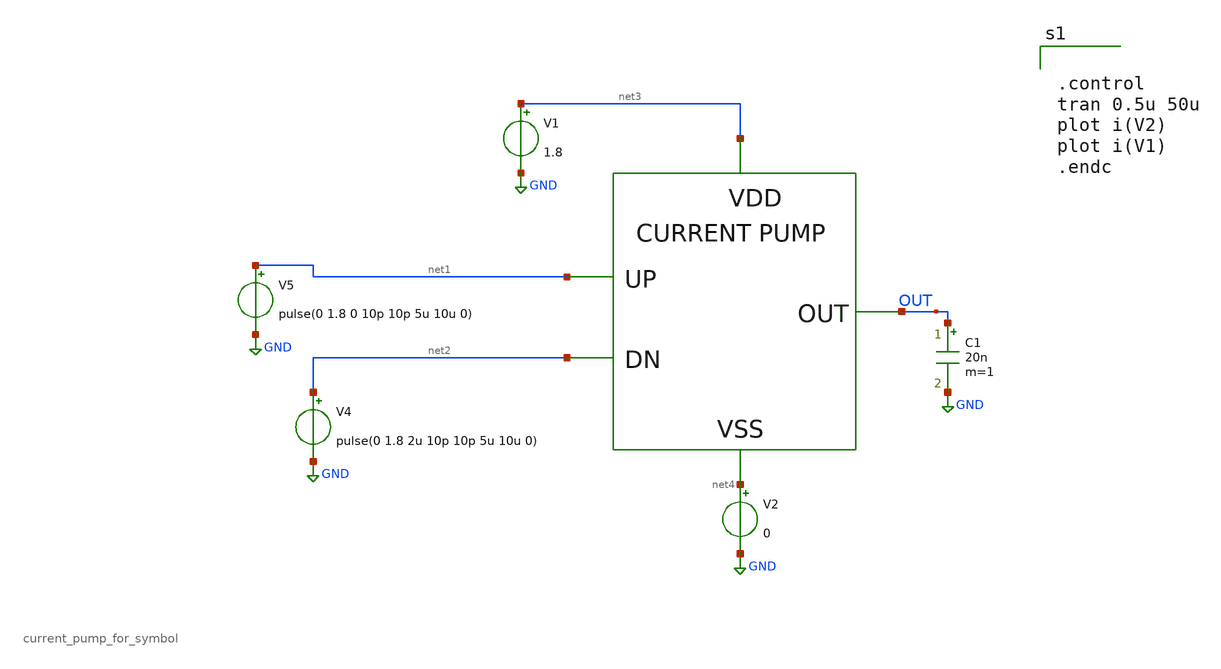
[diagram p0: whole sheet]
** sch_path: xschem/DC_DC_Converter_xschem/OTHERS/DC_DC_Converter_4/current_pump/current_pump_TB.sch
**.subckt current_pump_TB
X1 net1 OUT net3 net4 net2 current_pump_for_symbol
V5 net1 GND pulse(0 1.8 0 10p 10p 5u 10u 0)
V4 net2 GND pulse(0 1.8 2u 10p 10p 5u 10u 0)
V1 net3 GND 1.8
V2 net4 GND 0
C1 OUT GND 20n m=1
**** begin user architecture code


.control
tran 0.5u 50u
plot i(V2)
plot i(V1)
.endc



** opencircuitdesign pdks install
.lib $::SKYWATER_MODELS/sky130.lib.spice tt


**** end user architecture code
**.ends
.GLOBAL GND
.end
